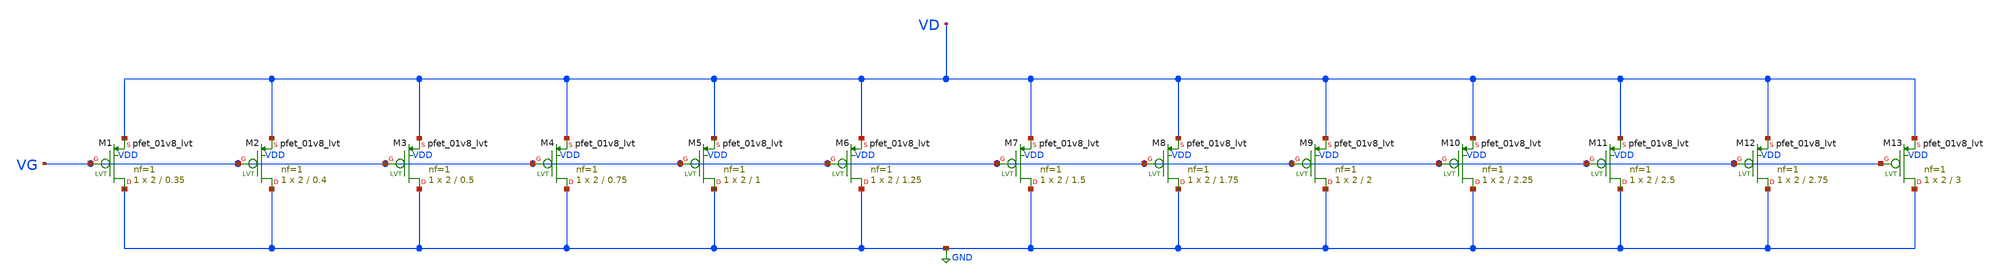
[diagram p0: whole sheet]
** sch_path: gmid Data/SKY130/pfet3_01v8_lvt/Pfet_lvt.sch
**.subckt Pfet_lvt
XM1 GND VG VD VDD sky130_fd_pr__pfet_01v8_lvt L=0.35 W=2 nf=1 ad='int((nf+1)/2) * W/nf * 0.29' as='int((nf+2)/2) * W/nf * 0.29'
+ pd='2*int((nf+1)/2) * (W/nf + 0.29)' ps='2*int((nf+2)/2) * (W/nf + 0.29)' nrd='0.29 / W' nrs='0.29 / W'
+ sa=0 sb=0 sd=0 mult=1 m=1
XM2 GND VG VD VDD sky130_fd_pr__pfet_01v8_lvt L=0.4 W=2 nf=1 ad='int((nf+1)/2) * W/nf * 0.29' as='int((nf+2)/2) * W/nf * 0.29'
+ pd='2*int((nf+1)/2) * (W/nf + 0.29)' ps='2*int((nf+2)/2) * (W/nf + 0.29)' nrd='0.29 / W' nrs='0.29 / W'
+ sa=0 sb=0 sd=0 mult=1 m=1
XM3 GND VG VD VDD sky130_fd_pr__pfet_01v8_lvt L=0.5 W=2 nf=1 ad='int((nf+1)/2) * W/nf * 0.29' as='int((nf+2)/2) * W/nf * 0.29'
+ pd='2*int((nf+1)/2) * (W/nf + 0.29)' ps='2*int((nf+2)/2) * (W/nf + 0.29)' nrd='0.29 / W' nrs='0.29 / W'
+ sa=0 sb=0 sd=0 mult=1 m=1
XM4 GND VG VD VDD sky130_fd_pr__pfet_01v8_lvt L=0.75 W=2 nf=1 ad='int((nf+1)/2) * W/nf * 0.29' as='int((nf+2)/2) * W/nf * 0.29'
+ pd='2*int((nf+1)/2) * (W/nf + 0.29)' ps='2*int((nf+2)/2) * (W/nf + 0.29)' nrd='0.29 / W' nrs='0.29 / W'
+ sa=0 sb=0 sd=0 mult=1 m=1
XM5 GND VG VD VDD sky130_fd_pr__pfet_01v8_lvt L=1 W=2 nf=1 ad='int((nf+1)/2) * W/nf * 0.29' as='int((nf+2)/2) * W/nf * 0.29'
+ pd='2*int((nf+1)/2) * (W/nf + 0.29)' ps='2*int((nf+2)/2) * (W/nf + 0.29)' nrd='0.29 / W' nrs='0.29 / W'
+ sa=0 sb=0 sd=0 mult=1 m=1
XM6 GND VG VD VDD sky130_fd_pr__pfet_01v8_lvt L=1.25 W=2 nf=1 ad='int((nf+1)/2) * W/nf * 0.29' as='int((nf+2)/2) * W/nf * 0.29'
+ pd='2*int((nf+1)/2) * (W/nf + 0.29)' ps='2*int((nf+2)/2) * (W/nf + 0.29)' nrd='0.29 / W' nrs='0.29 / W'
+ sa=0 sb=0 sd=0 mult=1 m=1
XM7 GND VG VD VDD sky130_fd_pr__pfet_01v8_lvt L=1.5 W=2 nf=1 ad='int((nf+1)/2) * W/nf * 0.29' as='int((nf+2)/2) * W/nf * 0.29'
+ pd='2*int((nf+1)/2) * (W/nf + 0.29)' ps='2*int((nf+2)/2) * (W/nf + 0.29)' nrd='0.29 / W' nrs='0.29 / W'
+ sa=0 sb=0 sd=0 mult=1 m=1
XM8 GND VG VD VDD sky130_fd_pr__pfet_01v8_lvt L=1.75 W=2 nf=1 ad='int((nf+1)/2) * W/nf * 0.29' as='int((nf+2)/2) * W/nf * 0.29'
+ pd='2*int((nf+1)/2) * (W/nf + 0.29)' ps='2*int((nf+2)/2) * (W/nf + 0.29)' nrd='0.29 / W' nrs='0.29 / W'
+ sa=0 sb=0 sd=0 mult=1 m=1
XM9 GND VG VD VDD sky130_fd_pr__pfet_01v8_lvt L=2 W=2 nf=1 ad='int((nf+1)/2) * W/nf * 0.29' as='int((nf+2)/2) * W/nf * 0.29'
+ pd='2*int((nf+1)/2) * (W/nf + 0.29)' ps='2*int((nf+2)/2) * (W/nf + 0.29)' nrd='0.29 / W' nrs='0.29 / W'
+ sa=0 sb=0 sd=0 mult=1 m=1
XM10 GND VG VD VDD sky130_fd_pr__pfet_01v8_lvt L=2.25 W=2 nf=1 ad='int((nf+1)/2) * W/nf * 0.29' as='int((nf+2)/2) * W/nf * 0.29'
+ pd='2*int((nf+1)/2) * (W/nf + 0.29)' ps='2*int((nf+2)/2) * (W/nf + 0.29)' nrd='0.29 / W' nrs='0.29 / W'
+ sa=0 sb=0 sd=0 mult=1 m=1
XM11 GND VG VD VDD sky130_fd_pr__pfet_01v8_lvt L=2.5 W=2 nf=1 ad='int((nf+1)/2) * W/nf * 0.29' as='int((nf+2)/2) * W/nf * 0.29'
+ pd='2*int((nf+1)/2) * (W/nf + 0.29)' ps='2*int((nf+2)/2) * (W/nf + 0.29)' nrd='0.29 / W' nrs='0.29 / W'
+ sa=0 sb=0 sd=0 mult=1 m=1
XM12 GND VG VD VDD sky130_fd_pr__pfet_01v8_lvt L=2.75 W=2 nf=1 ad='int((nf+1)/2) * W/nf * 0.29' as='int((nf+2)/2) * W/nf * 0.29'
+ pd='2*int((nf+1)/2) * (W/nf + 0.29)' ps='2*int((nf+2)/2) * (W/nf + 0.29)' nrd='0.29 / W' nrs='0.29 / W'
+ sa=0 sb=0 sd=0 mult=1 m=1
XM13 GND VG VD VDD sky130_fd_pr__pfet_01v8_lvt L=3 W=2 nf=1 ad='int((nf+1)/2) * W/nf * 0.29' as='int((nf+2)/2) * W/nf * 0.29'
+ pd='2*int((nf+1)/2) * (W/nf + 0.29)' ps='2*int((nf+2)/2) * (W/nf + 0.29)' nrd='0.29 / W' nrs='0.29 / W'
+ sa=0 sb=0 sd=0 mult=1 m=1
**.ends
.GLOBAL GND
.end
